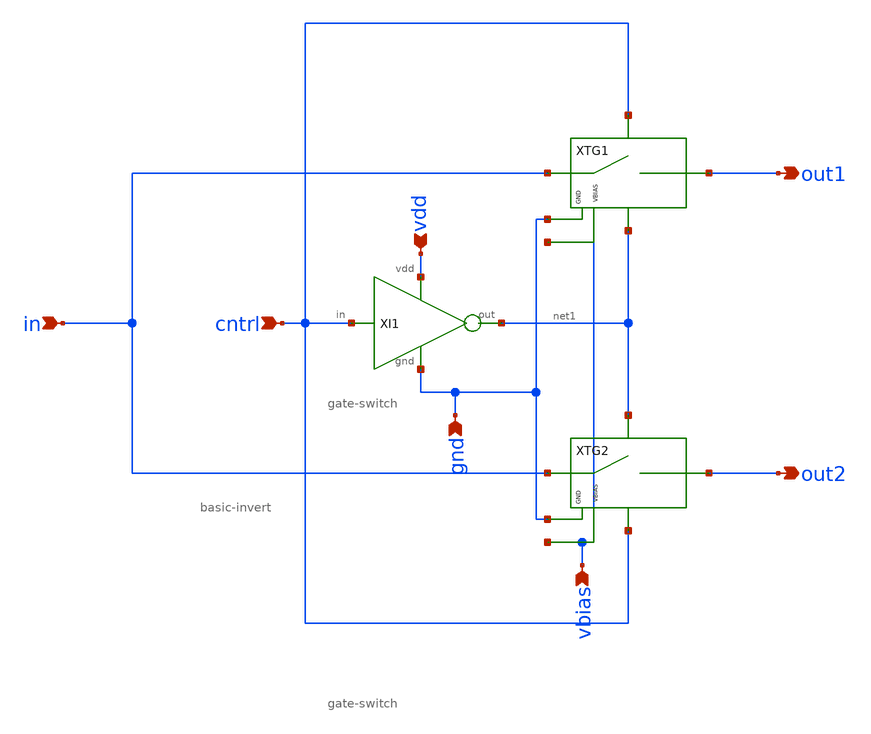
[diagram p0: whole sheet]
** sch_path: xschem/attenuator/transgate-full.sch
**.subckt transgate-full cntrl vdd in gnd vbias out2 out1
*.ipin cntrl
*.ipin vdd
*.ipin in
*.ipin gnd
*.ipin vbias
*.opin out2
*.opin out1
XI1 vdd gnd net1 cntrl basic-invert
XTG1 in out1 gnd vbias net1 cntrl gate-switch
XTG2 in out2 gnd vbias cntrl net1 gate-switch
**** begin user architecture code
 ** manual skywater pdks install (with patches applied)
* .lib $::SKYWATER_MODELS/models/sky130.lib.spice tt

** opencircuitdesign pdks install
.lib $::SKYWATER_MODELS/sky130.lib.spice tt

.param mc_mm_switch=0
.param mc_pr_switch=0

**** end user architecture code
**.ends

* expanding   symbol:  basic-invert.sym # of pins=4
** sym_path: xschem/attenuator/basic-invert.sym
** sch_path: xschem/attenuator/basic-invert.sch
.subckt basic-invert vdd gnd out in
*.ipin in
*.ipin gnd
*.ipin vdd
*.opin out
XM1 out in gnd gnd sky130_fd_pr__nfet_01v8 L=0.15 W=1 nf=1 ad='int((nf+1)/2) * W/nf * 0.29' as='int((nf+2)/2) * W/nf * 0.29'
+ pd='2*int((nf+1)/2) * (W/nf + 0.29)' ps='2*int((nf+2)/2) * (W/nf + 0.29)' nrd='0.29 / W' nrs='0.29 / W'
+ sa=0 sb=0 sd=0 mult=1 m=1
XM2 out in vdd vdd sky130_fd_pr__pfet_01v8 L=0.15 W=1 nf=1 ad='int((nf+1)/2) * W/nf * 0.29' as='int((nf+2)/2) * W/nf * 0.29'
+ pd='2*int((nf+1)/2) * (W/nf + 0.29)' ps='2*int((nf+2)/2) * (W/nf + 0.29)' nrd='0.29 / W' nrs='0.29 / W'
+ sa=0 sb=0 sd=0 mult=1 m=1
.ends


* expanding   symbol:  gate-switch.sym # of pins=6
** sym_path: xschem/attenuator/gate-switch.sym
** sch_path: xschem/attenuator/gate-switch.sch
.subckt gate-switch in out gnd vbias cntrl2 cntrl1
*.ipin in
*.ipin vbias
*.ipin gnd
*.opin out
*.ipin cntrl1
*.ipin cntrl2
XM5 in cntrl2 out vbias sky130_fd_pr__pfet_01v8 L=0.15 W=1 nf=1 ad='int((nf+1)/2) * W/nf * 0.29' as='int((nf+2)/2) * W/nf * 0.29'
+ pd='2*int((nf+1)/2) * (W/nf + 0.29)' ps='2*int((nf+2)/2) * (W/nf + 0.29)' nrd='0.29 / W' nrs='0.29 / W'
+ sa=0 sb=0 sd=0 mult=1 m=1
XM6 out cntrl1 in gnd sky130_fd_pr__nfet_01v8 L=0.15 W=1 nf=1 ad='int((nf+1)/2) * W/nf * 0.29' as='int((nf+2)/2) * W/nf * 0.29'
+ pd='2*int((nf+1)/2) * (W/nf + 0.29)' ps='2*int((nf+2)/2) * (W/nf + 0.29)' nrd='0.29 / W' nrs='0.29 / W'
+ sa=0 sb=0 sd=0 mult=1 m=1
.ends

.end
